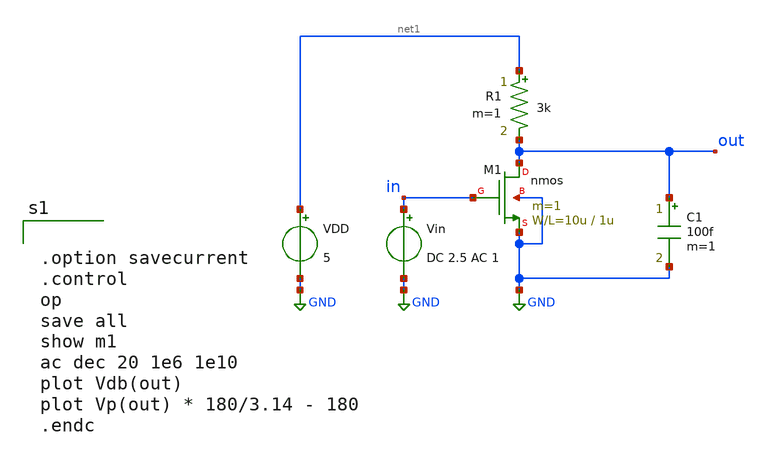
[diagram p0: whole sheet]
** sch_path: member_project/GroupWork/Team_masahiro/nfet_common_source_AC.sch
**.subckt nfet_common_source_AC
M1 out in GND GND nmos L=1u W=10u m=1
R1 net1 out 3k m=1
VDD net1 GND 5
Vin in GND DC 2.5 AC 1
C1 out GND 100f m=1
**** begin user architecture code
 .include $::LIB/mos.lib
.include $::LIB/passive.lib
.include $::LIB/diode.lib


.option savecurrent
.control
op
save all
show m1
ac dec 20 1e6 1e10
plot Vdb(out)
plot Vp(out) * 180/3.14 - 180
.endc


**** end user architecture code
**.ends
.GLOBAL GND
.end
